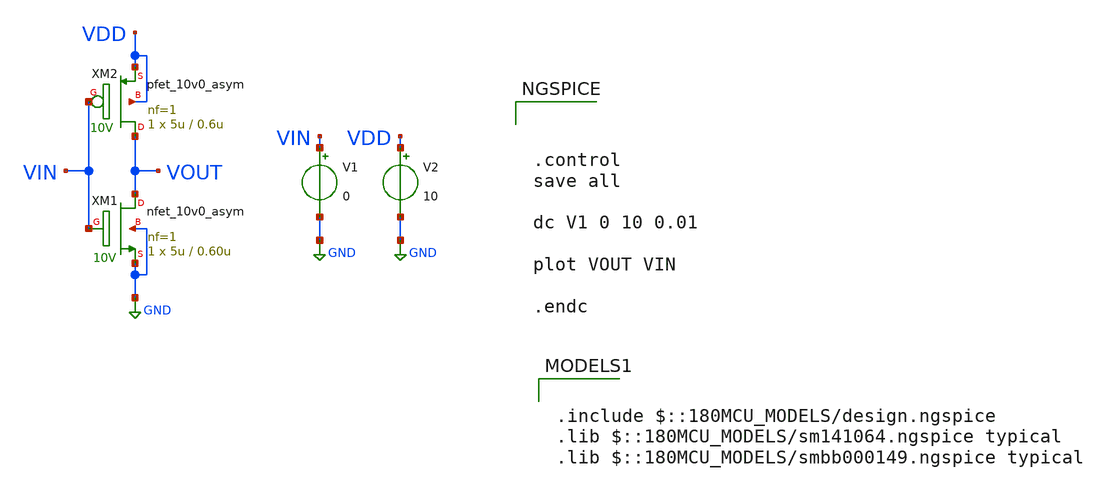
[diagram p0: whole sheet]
** sch_path: week01_mosfet_cmos/tugas2_cmos_inverter/cmos-inverter2.sch
**.subckt cmos-inverter2
XM1 VOUT VIN GND GND nfet_10v0_asym L=0.60u W=5u nf=1 ad='W * 1.48u' as='W * 0.48u' pd='2 * (W + 1.48u)'
+ ps='2 * (W + 0.48u)' nrd=0 nrs=0 sa=0 sb=0 sd=0 m=1
XM2 VOUT VIN VDD VDD pfet_10v0_asym L=0.6u W=5u nf=1 ad='W * 1.78u' as='W * 0.48u' pd='2 * (W + 1.78u)'
+ ps='2 * (W + 0.48u)' nrd=0 nrs=0 sa=0 sb=0 sd=0 m=1
V1 VIN GND 0
V2 VDD GND 10
**** begin user architecture code



.control
save all

dc V1 0 10 0.01

plot VOUT VIN

.endc



.include $::180MCU_MODELS/design.ngspice
.lib $::180MCU_MODELS/sm141064.ngspice typical
.lib $::180MCU_MODELS/smbb000149.ngspice typical

**** end user architecture code
**.ends
.GLOBAL GND
.end
